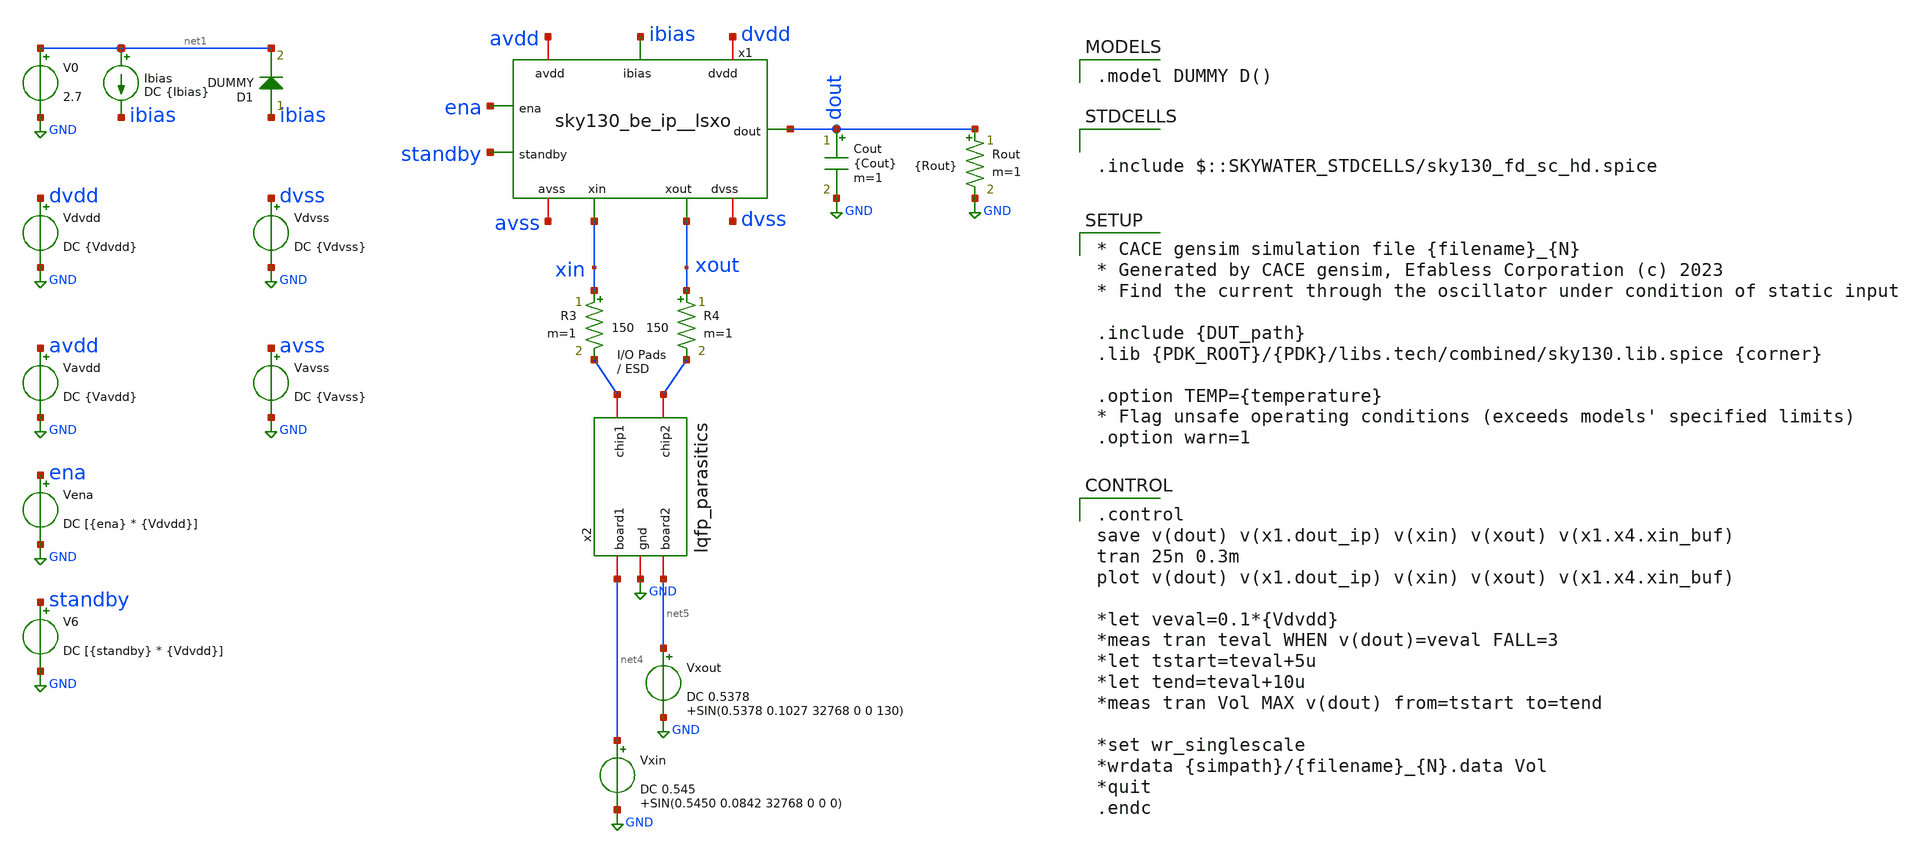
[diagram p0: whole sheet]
** sch_path: cace/tb_vol.sch

.include $::SKYWATER_STDCELLS/sky130_fd_sc_hd.spice

**.subckt tb_vol
Vdvdd dvdd GND DC {Vdvdd}
Vavdd avdd GND DC {Vavdd}
Ibias net1 ibias DC {Ibias}
Cout dout GND {Cout} m=1
V0 net1 GND 2.7
V6 standby GND DC [{standby} * {Vdvdd}]
R3 xin net2 150 m=1
R4 xout net3 150 m=1
x2 net3 net2 GND net4 net5 lqfp_parasitics
Vena ena GND DC [{ena} * {Vdvdd}]
D1 ibias net1 DUMMY area=100
x1 avdd avss dvdd dvss ibias ena standby dout xin xout sky130_be_ip__lsxo
Vdvss dvss GND DC {Vdvss}
Vavss avss GND DC {Vavss}
Rout dout GND {Rout} m=1
Vxout net5 GND DC 0.5378 SIN(0.5378 0.1027 32768 0 0 130)
Vxin net4 GND DC 0.545 SIN(0.5450 0.0842 32768 0 0 0)
**** begin user architecture code

.model DUMMY D()


.control
save v(dout) v(x1.dout_ip) v(xin) v(xout) v(x1.x4.xin_buf)
tran 25n 0.3m
plot v(dout) v(x1.dout_ip) v(xin) v(xout) v(x1.x4.xin_buf)

*let veval=0.1*{Vdvdd}
*meas tran teval WHEN v(dout)=veval FALL=3
*let tstart=teval+5u
*let tend=teval+10u
*meas tran Vol MAX v(dout) from=tstart to=tend

*set wr_singlescale
*wrdata {simpath}/{filename}_{N}.data Vol
*quit
.endc



* CACE gensim simulation file {filename}_{N}
* Generated by CACE gensim, Efabless Corporation (c) 2023
* Find the current through the oscillator under condition of static input

.include {DUT_path}
.lib {PDK_ROOT}/{PDK}/libs.tech/combined/sky130.lib.spice {corner}

.option TEMP={temperature}
* Flag unsafe operating conditions (exceeds models' specified limits)
.option warn=1


**** end user architecture code
**.ends
.GLOBAL GND
.end
